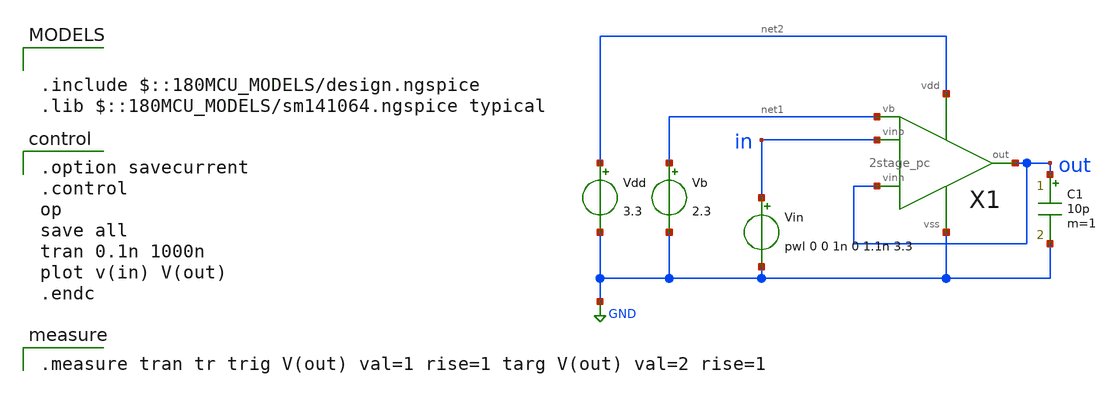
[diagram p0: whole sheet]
** sch_path: opamp/2stage_pc_tran.sch
**.subckt 2stage_pc_tran
Vdd net2 GND 3.3
Vb net1 GND 2.3
C1 out GND 10p m=1
Vin in GND pwl 0 0 1n 0 1.1n 3.3
X1 in out net1 out net2 GND 2stage_pc
**** begin user architecture code

.include $::180MCU_MODELS/design.ngspice
.lib $::180MCU_MODELS/sm141064.ngspice typical


.option savecurrent
.control
op
save all
tran 0.1n 1000n
plot v(in) V(out)
.endc


.measure tran tr trig V(out) val=1 rise=1 targ V(out) val=2 rise=1

**** end user architecture code
**.ends
.GLOBAL GND
.end
